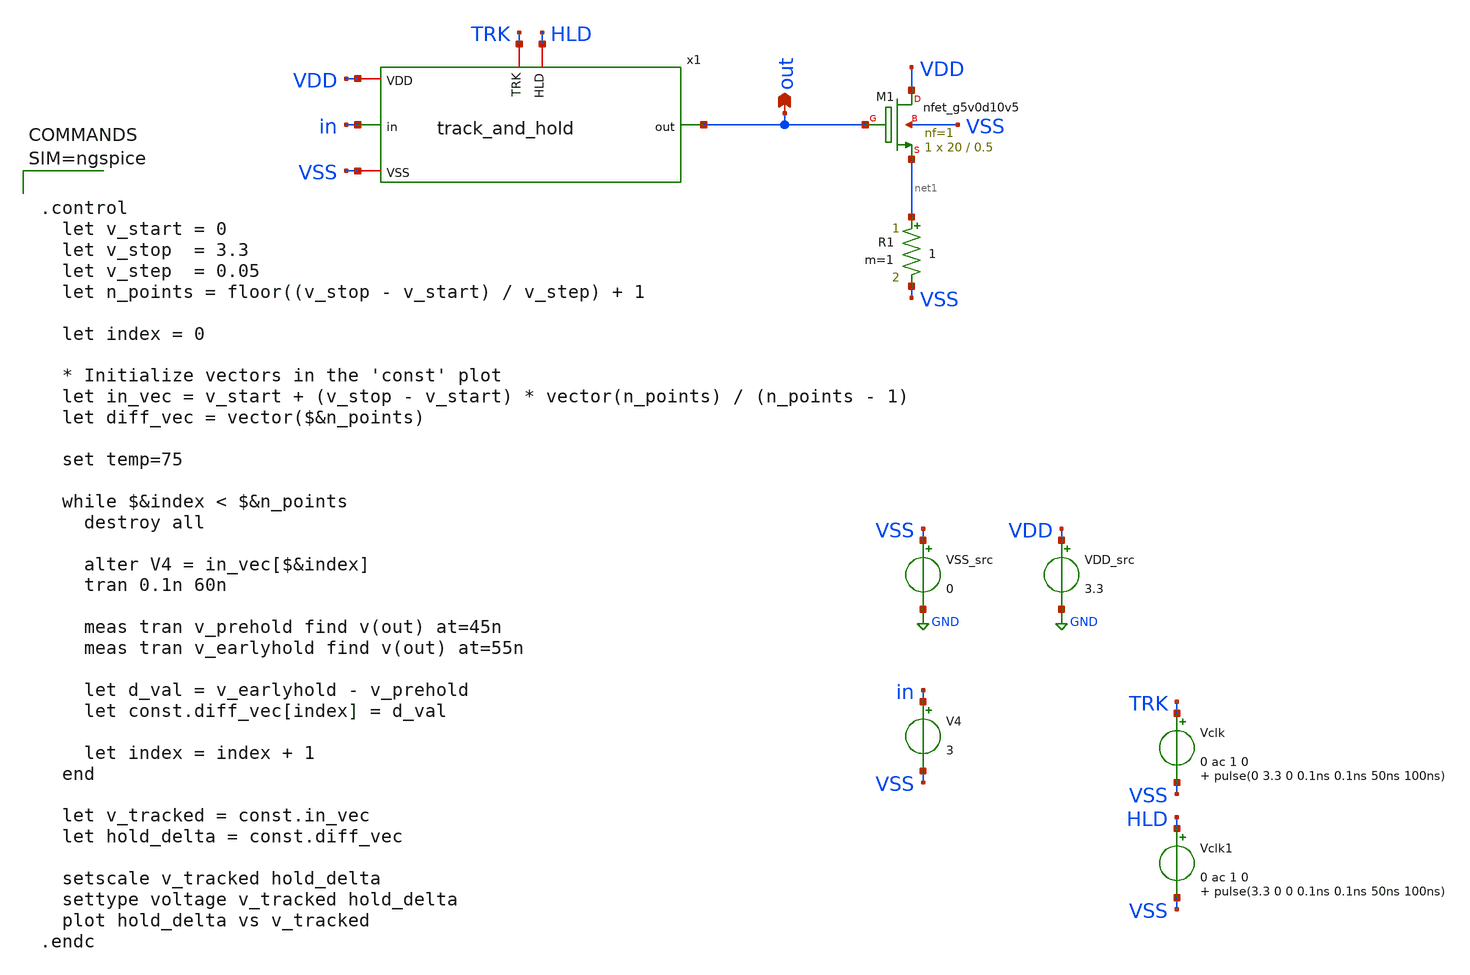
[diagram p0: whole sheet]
** sch_path: xschem/hold_testbench.sch
**.subckt hold_testbench out
*.opin out
VDD_src VDD GND 3.3
VSS_src VSS GND 0
V4 in VSS 3
XM1 VDD out net1 VSS sky130_fd_pr__nfet_g5v0d10v5 L=0.5 W=20 nf=1 ad='int((nf+1)/2) * W/nf * 0.29' as='int((nf+2)/2) * W/nf * 0.29'
+ pd='2*int((nf+1)/2) * (W/nf + 0.29)' ps='2*int((nf+2)/2) * (W/nf + 0.29)' nrd='0.29 / W' nrs='0.29 / W'
+ sa=0 sb=0 sd=0 mult=1 m=1
R1 net1 VSS 1 m=1
Vclk TRK VSS 0 ac 1 0 pulse(0 3.3 0 0.1ns 0.1ns 50ns 100ns)
Vclk1 HLD VSS 0 ac 1 0 pulse(3.3 0 0 0.1ns 0.1ns 50ns 100ns)
x1 HLD TRK VDD VSS out in track_and_hold
**** begin user architecture code

** opencircuitdesign pdks install
.lib $::SKYWATER_MODELS/sky130.lib.spice ss





.control
  let v_start = 0
  let v_stop  = 3.3
  let v_step  = 0.05
  let n_points = floor((v_stop - v_start) / v_step) + 1

  let index = 0

  * Initialize vectors in the 'const' plot
  let in_vec = v_start + (v_stop - v_start) * vector(n_points) / (n_points - 1)
  let diff_vec = vector($&n_points)

  set temp=75

  while $&index < $&n_points
    destroy all

    alter V4 = in_vec[$&index]
    tran 0.1n 60n

    meas tran v_prehold find v(out) at=45n
    meas tran v_earlyhold find v(out) at=55n

    let d_val = v_earlyhold - v_prehold
    let const.diff_vec[index] = d_val

    let index = index + 1
  end

  let v_tracked = const.in_vec
  let hold_delta = const.diff_vec

  setscale v_tracked hold_delta
  settype voltage v_tracked hold_delta
  plot hold_delta vs v_tracked
.endc



**** end user architecture code
**.ends

* expanding   symbol:  track_and_hold.sym # of pins=6
** sym_path: xschem/track_and_hold.sym
** sch_path: xschem/track_and_hold.sch
.subckt track_and_hold HLD TRK VDD VSS out in
*.iopin VSS
*.iopin VDD
*.ipin in
*.opin out
*.iopin TRK
*.iopin HLD
XC1 out VSS sky130_fd_pr__cap_mim_m3_1 W=5 L=5 MF=1 m=1
V1 net2 net5 3.3
XM1 out net1 in VSS sky130_fd_pr__nfet_g5v0d10v5 L=0.5 W=1 nf=1 ad='int((nf+1)/2) * W/nf * 0.29' as='int((nf+2)/2) * W/nf * 0.29'
+ pd='2*int((nf+1)/2) * (W/nf + 0.29)' ps='2*int((nf+2)/2) * (W/nf + 0.29)' nrd='0.29 / W' nrs='0.29 / W'
+ sa=0 sb=0 sd=0 mult=1 m=1
R1 VDD VSS 1G m=1
**** begin user architecture code



.model switch1 sw vt=1.65 vh=0 ron=1 roff=1G



**** end user architecture code
V2 net6 net3 3.3
XM1p out net4 in VDD sky130_fd_pr__pfet_g5v0d10v5 L=0.5 W=1.28 nf=1 ad='int((nf+1)/2) * W/nf * 0.29'
+ as='int((nf+2)/2) * W/nf * 0.29' pd='2*int((nf+1)/2) * (W/nf + 0.29)' ps='2*int((nf+2)/2) * (W/nf + 0.29)'
+ nrd='0.29 / W' nrs='0.29 / W' sa=0 sb=0 sd=0 mult=1 m=1
XM4 VSS HLD net1 VSS sky130_fd_pr__nfet_g5v0d10v5 L=0.5 W=1 nf=1 ad='int((nf+1)/2) * W/nf * 0.29' as='int((nf+2)/2) * W/nf * 0.29'
+ pd='2*int((nf+1)/2) * (W/nf + 0.29)' ps='2*int((nf+2)/2) * (W/nf + 0.29)' nrd='0.29 / W' nrs='0.29 / W'
+ sa=0 sb=0 sd=0 mult=1 m=1
XM4p net4 TRK VDD VDD sky130_fd_pr__pfet_g5v0d10v5 L=0.5 W=2 nf=1 ad='int((nf+1)/2) * W/nf * 0.29' as='int((nf+2)/2) * W/nf * 0.29'
+ pd='2*int((nf+1)/2) * (W/nf + 0.29)' ps='2*int((nf+2)/2) * (W/nf + 0.29)' nrd='0.29 / W' nrs='0.29 / W'
+ sa=0 sb=0 sd=0 mult=1 m=1
XM2 net1 HLD net2 net2 sky130_fd_pr__pfet_g5v0d10v5 L=0.5 W=2 nf=1 ad='int((nf+1)/2) * W/nf * 0.29' as='int((nf+2)/2) * W/nf * 0.29'
+ pd='2*int((nf+1)/2) * (W/nf + 0.29)' ps='2*int((nf+2)/2) * (W/nf + 0.29)' nrd='0.29 / W' nrs='0.29 / W'
+ sa=0 sb=0 sd=0 mult=1 m=1
XM2p net3 TRK net4 net3 sky130_fd_pr__nfet_g5v0d10v5 L=0.5 W=1 nf=1 ad='int((nf+1)/2) * W/nf * 0.29'
+ as='int((nf+2)/2) * W/nf * 0.29' pd='2*int((nf+1)/2) * (W/nf + 0.29)' ps='2*int((nf+2)/2) * (W/nf + 0.29)'
+ nrd='0.29 / W' nrs='0.29 / W' sa=0 sb=0 sd=0 mult=1 m=1
XM3 in net1 net5 VSS sky130_fd_pr__nfet_g5v0d10v5 L=0.5 W=1 nf=1 ad='int((nf+1)/2) * W/nf * 0.29' as='int((nf+2)/2) * W/nf * 0.29'
+ pd='2*int((nf+1)/2) * (W/nf + 0.29)' ps='2*int((nf+2)/2) * (W/nf + 0.29)' nrd='0.29 / W' nrs='0.29 / W'
+ sa=0 sb=0 sd=0 mult=1 m=1
XM6 net5 HLD VSS VSS sky130_fd_pr__nfet_g5v0d10v5 L=0.5 W=1 nf=1 ad='int((nf+1)/2) * W/nf * 0.29' as='int((nf+2)/2) * W/nf * 0.29'
+ pd='2*int((nf+1)/2) * (W/nf + 0.29)' ps='2*int((nf+2)/2) * (W/nf + 0.29)' nrd='0.29 / W' nrs='0.29 / W'
+ sa=0 sb=0 sd=0 mult=1 m=1
XM3p net6 net4 in VDD sky130_fd_pr__pfet_g5v0d10v5 L=0.5 W=2 nf=1 ad='int((nf+1)/2) * W/nf * 0.29' as='int((nf+2)/2) * W/nf * 0.29'
+ pd='2*int((nf+1)/2) * (W/nf + 0.29)' ps='2*int((nf+2)/2) * (W/nf + 0.29)' nrd='0.29 / W' nrs='0.29 / W'
+ sa=0 sb=0 sd=0 mult=1 m=1
XM6p VDD TRK net6 VDD sky130_fd_pr__pfet_g5v0d10v5 L=0.5 W=2 nf=1 ad='int((nf+1)/2) * W/nf * 0.29' as='int((nf+2)/2) * W/nf * 0.29'
+ pd='2*int((nf+1)/2) * (W/nf + 0.29)' ps='2*int((nf+2)/2) * (W/nf + 0.29)' nrd='0.29 / W' nrs='0.29 / W'
+ sa=0 sb=0 sd=0 mult=1 m=1
.ends

.GLOBAL GND
.end
